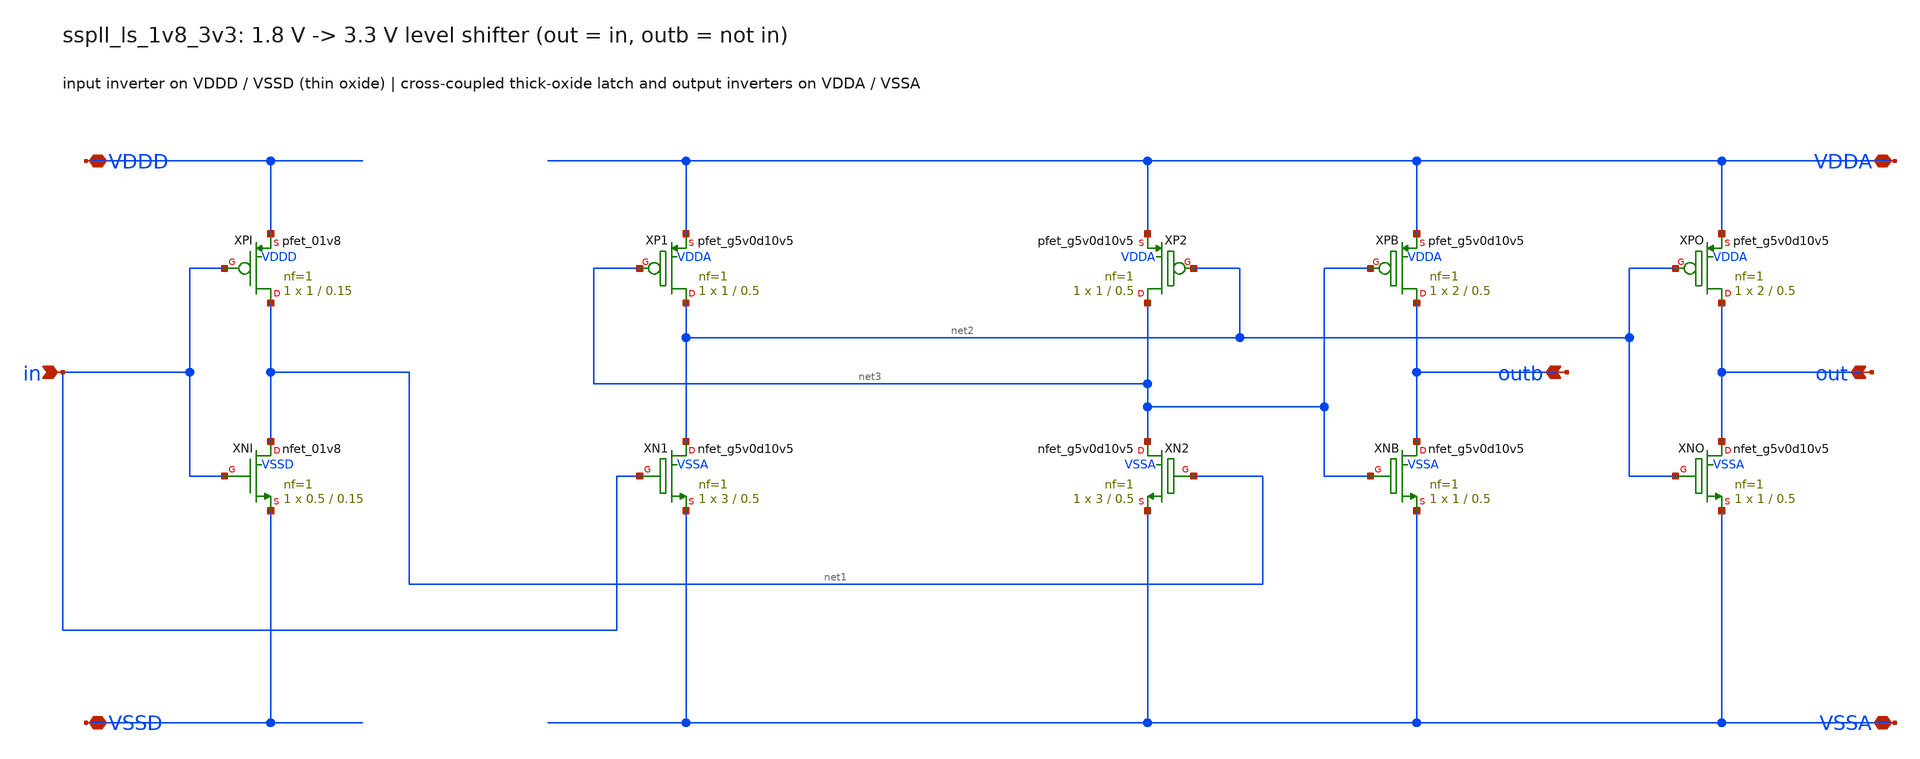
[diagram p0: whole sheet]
** sch_path: xschem/cco_hv/sspll_ls_1v8_3v3.sch
**.subckt sspll_ls_1v8_3v3 VDDD VDDA VSSD VSSA in outb out
*.iopin VDDD
*.iopin VDDA
*.iopin VSSD
*.iopin VSSA
*.ipin in
*.opin outb
*.opin out
XXPI net1 in VDDD VDDD sky130_fd_pr__pfet_01v8 L=0.15 W=1 nf=1 ad='int((nf+1)/2) * W/nf * 0.29' as='int((nf+2)/2) * W/nf * 0.29'
+ pd='2*int((nf+1)/2) * (W/nf + 0.29)' ps='2*int((nf+2)/2) * (W/nf + 0.29)' nrd='0.29 / W' nrs='0.29 / W'
+ sa=0 sb=0 sd=0 mult=1 m=1
XXNI net1 in VSSD VSSD sky130_fd_pr__nfet_01v8 L=0.15 W=0.5 nf=1 ad='int((nf+1)/2) * W/nf * 0.29' as='int((nf+2)/2) * W/nf * 0.29'
+ pd='2*int((nf+1)/2) * (W/nf + 0.29)' ps='2*int((nf+2)/2) * (W/nf + 0.29)' nrd='0.29 / W' nrs='0.29 / W'
+ sa=0 sb=0 sd=0 mult=1 m=1
XXP1 net2 net3 VDDA VDDA sky130_fd_pr__pfet_g5v0d10v5 L=0.5 W=1 nf=1 ad='int((nf+1)/2) * W/nf * 0.29'
+ as='int((nf+2)/2) * W/nf * 0.29' pd='2*int((nf+1)/2) * (W/nf + 0.29)' ps='2*int((nf+2)/2) * (W/nf + 0.29)'
+ nrd='0.29 / W' nrs='0.29 / W' sa=0 sb=0 sd=0 mult=1 m=1
XXP2 net3 net2 VDDA VDDA sky130_fd_pr__pfet_g5v0d10v5 L=0.5 W=1 nf=1 ad='int((nf+1)/2) * W/nf * 0.29'
+ as='int((nf+2)/2) * W/nf * 0.29' pd='2*int((nf+1)/2) * (W/nf + 0.29)' ps='2*int((nf+2)/2) * (W/nf + 0.29)'
+ nrd='0.29 / W' nrs='0.29 / W' sa=0 sb=0 sd=0 mult=1 m=1
XXN1 net2 in VSSA VSSA sky130_fd_pr__nfet_g5v0d10v5 L=0.5 W=3 nf=1 ad='int((nf+1)/2) * W/nf * 0.29' as='int((nf+2)/2) * W/nf * 0.29'
+ pd='2*int((nf+1)/2) * (W/nf + 0.29)' ps='2*int((nf+2)/2) * (W/nf + 0.29)' nrd='0.29 / W' nrs='0.29 / W'
+ sa=0 sb=0 sd=0 mult=1 m=1
XXN2 net3 net1 VSSA VSSA sky130_fd_pr__nfet_g5v0d10v5 L=0.5 W=3 nf=1 ad='int((nf+1)/2) * W/nf * 0.29'
+ as='int((nf+2)/2) * W/nf * 0.29' pd='2*int((nf+1)/2) * (W/nf + 0.29)' ps='2*int((nf+2)/2) * (W/nf + 0.29)'
+ nrd='0.29 / W' nrs='0.29 / W' sa=0 sb=0 sd=0 mult=1 m=1
XXPB outb net3 VDDA VDDA sky130_fd_pr__pfet_g5v0d10v5 L=0.5 W=2 nf=1 ad='int((nf+1)/2) * W/nf * 0.29'
+ as='int((nf+2)/2) * W/nf * 0.29' pd='2*int((nf+1)/2) * (W/nf + 0.29)' ps='2*int((nf+2)/2) * (W/nf + 0.29)'
+ nrd='0.29 / W' nrs='0.29 / W' sa=0 sb=0 sd=0 mult=1 m=1
XXNB outb net3 VSSA VSSA sky130_fd_pr__nfet_g5v0d10v5 L=0.5 W=1 nf=1 ad='int((nf+1)/2) * W/nf * 0.29'
+ as='int((nf+2)/2) * W/nf * 0.29' pd='2*int((nf+1)/2) * (W/nf + 0.29)' ps='2*int((nf+2)/2) * (W/nf + 0.29)'
+ nrd='0.29 / W' nrs='0.29 / W' sa=0 sb=0 sd=0 mult=1 m=1
XXPO out net2 VDDA VDDA sky130_fd_pr__pfet_g5v0d10v5 L=0.5 W=2 nf=1 ad='int((nf+1)/2) * W/nf * 0.29'
+ as='int((nf+2)/2) * W/nf * 0.29' pd='2*int((nf+1)/2) * (W/nf + 0.29)' ps='2*int((nf+2)/2) * (W/nf + 0.29)'
+ nrd='0.29 / W' nrs='0.29 / W' sa=0 sb=0 sd=0 mult=1 m=1
XXNO out net2 VSSA VSSA sky130_fd_pr__nfet_g5v0d10v5 L=0.5 W=1 nf=1 ad='int((nf+1)/2) * W/nf * 0.29'
+ as='int((nf+2)/2) * W/nf * 0.29' pd='2*int((nf+1)/2) * (W/nf + 0.29)' ps='2*int((nf+2)/2) * (W/nf + 0.29)'
+ nrd='0.29 / W' nrs='0.29 / W' sa=0 sb=0 sd=0 mult=1 m=1
**.ends
.end
